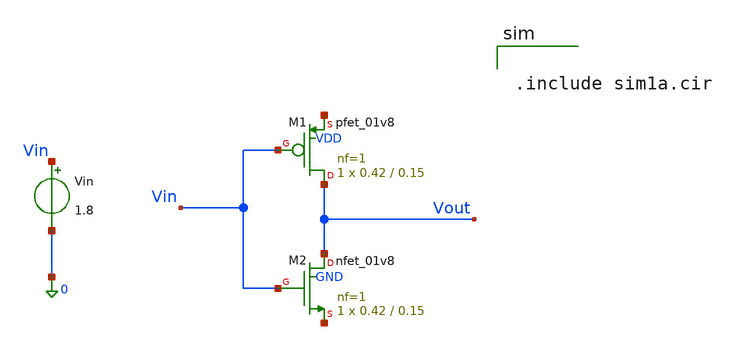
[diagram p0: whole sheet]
** sch_path: assignments/assignment2/assign1a.sch
**.subckt assign1a
Vin Vin 0 1.8
XM1 Vout Vin net1 VDD sky130_fd_pr__pfet_01v8 L=0.15 W=0.42 nf=1 ad='int((nf+1)/2) * W/nf * 0.29' as='int((nf+2)/2) * W/nf * 0.29'
+ pd='2*int((nf+1)/2) * (W/nf + 0.29)' ps='2*int((nf+2)/2) * (W/nf + 0.29)' nrd='0.29 / W' nrs='0.29 / W'
+ sa=0 sb=0 sd=0 mult=1 m=1
XM2 Vout Vin net2 GND sky130_fd_pr__nfet_01v8 L=0.15 W=0.42 nf=1 ad='int((nf+1)/2) * W/nf * 0.29' as='int((nf+2)/2) * W/nf * 0.29'
+ pd='2*int((nf+1)/2) * (W/nf + 0.29)' ps='2*int((nf+2)/2) * (W/nf + 0.29)' nrd='0.29 / W' nrs='0.29 / W'
+ sa=0 sb=0 sd=0 mult=1 m=1
**** begin user architecture code


.include sim1a.cir


**** end user architecture code
**.ends
.end
